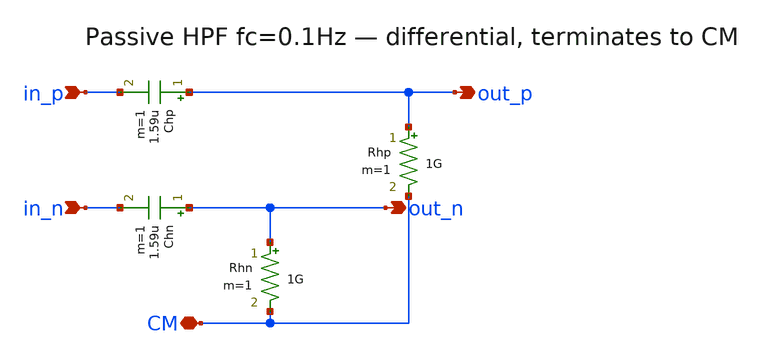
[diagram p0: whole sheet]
** sch_path: ps-filters/hpf.sch
**.subckt hpf in_p in_n out_p out_n CM
*.ipin in_p
*.ipin in_n
*.opin out_p
*.opin out_n
*.iopin CM
Chp out_p in_p 1.59u m=1
Chn out_n in_n 1.59u m=1
Rhp out_p CM 1G m=1
Rhn out_n CM 1G m=1
**.ends
.end
